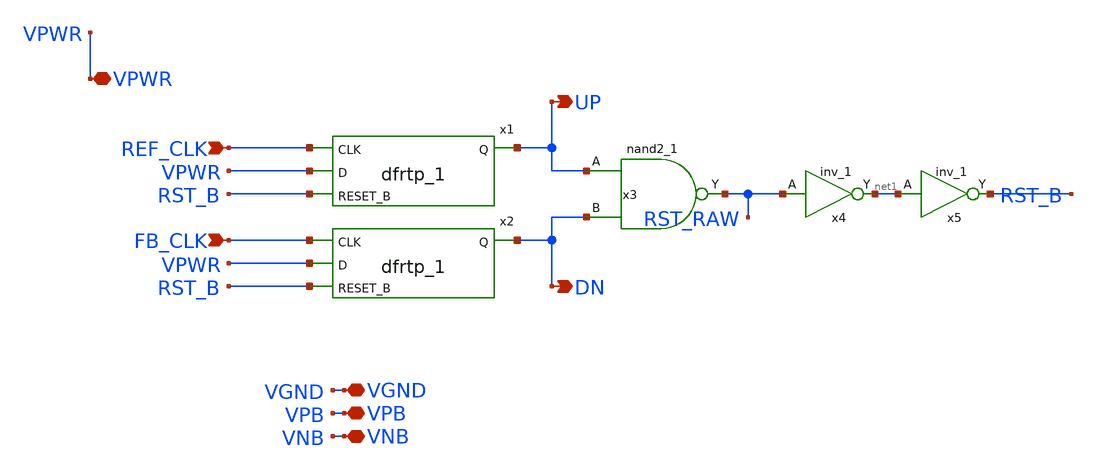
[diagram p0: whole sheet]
** sch_path: pfd.sch
**.subckt pfd REF_CLK FB_CLK VGND VPB VNB VPWR UP DN
*.ipin REF_CLK
*.ipin FB_CLK
*.iopin VGND
*.iopin VPB
*.iopin VNB
*.iopin VPWR
*.opin UP
*.opin DN
x1 REF_CLK VPWR RST_B VGND VNB VPB VPWR UP sky130_fd_sc_hd__dfrtp_1
x2 FB_CLK VPWR RST_B VGND VNB VPB VPWR DN sky130_fd_sc_hd__dfrtp_1
x3 UP DN VGND VNB VPB VPWR RST_RAW sky130_fd_sc_hd__nand2_1
x4 RST_RAW VGND VNB VPB VPWR net1 sky130_fd_sc_hd__inv_1
x5 net1 VGND VNB VPB VPWR RST_B sky130_fd_sc_hd__inv_1
**.ends
.end
